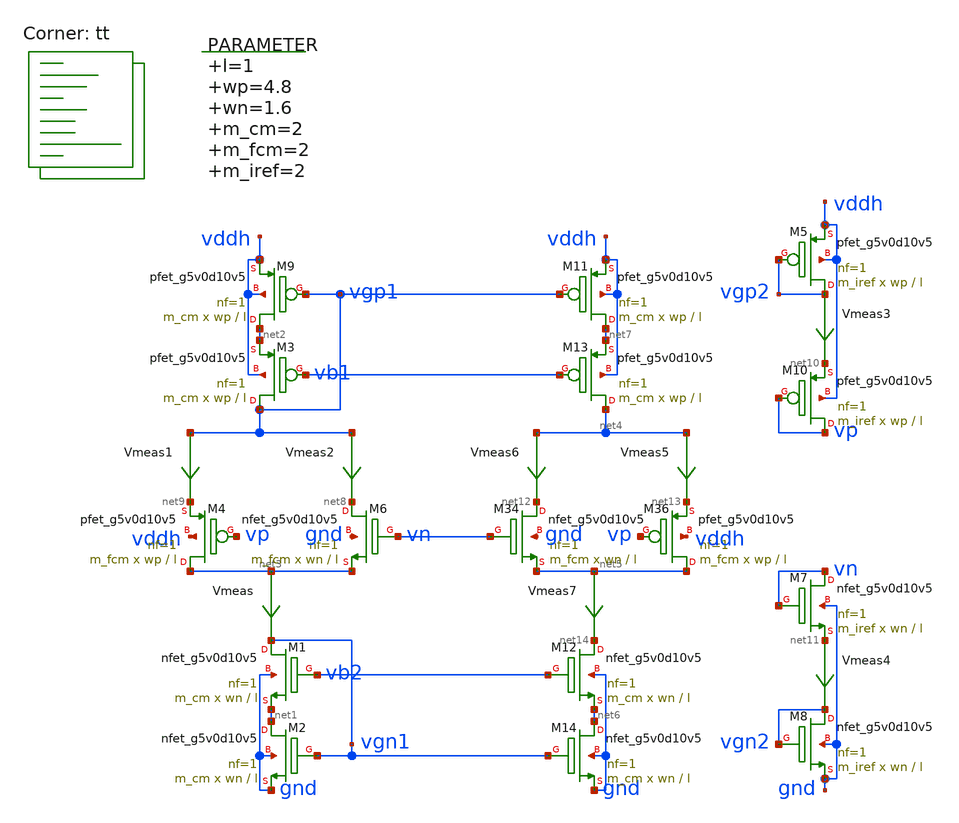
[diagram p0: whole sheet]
** sch_path: xschem/op_amp_lv_cm.sch
**.subckt op_amp_lv_cm
Vmeas net3 vgn1 0
.save i(vmeas)
XM9 net2 vgp1 vddh vddh sky130_fd_pr__pfet_g5v0d10v5 L=l W=wp nf=1 ad='int((nf+1)/2) * W/nf * 0.29' as='int((nf+2)/2) * W/nf * 0.29'
+ pd='2*int((nf+1)/2) * (W/nf + 0.29)' ps='2*int((nf+2)/2) * (W/nf + 0.29)' nrd='0.29 / W' nrs='0.29 / W'
+ sa=0 sb=0 sd=0 mult=m_cm m=m_cm
XM6 net8 vn net3 gnd sky130_fd_pr__nfet_g5v0d10v5 L=l W=wn nf=1 ad='int((nf+1)/2) * W/nf * 0.29' as='int((nf+2)/2) * W/nf * 0.29'
+ pd='2*int((nf+1)/2) * (W/nf + 0.29)' ps='2*int((nf+2)/2) * (W/nf + 0.29)' nrd='0.29 / W' nrs='0.29 / W'
+ sa=0 sb=0 sd=0 mult=m_fcm m=m_fcm
Vmeas1 vgp1 net9 0
.save i(vmeas1)
Vmeas2 vgp1 net8 0
.save i(vmeas2)
Vmeas3 vgp2 net10 0
.save i(vmeas3)
Vmeas4 net11 vgn2 0
.save i(vmeas4)
.param l=1 wp=4.8 wn=1.6 m_cm=2 m_fcm=2 m_iref=2
XM4 net3 vp net9 vddh sky130_fd_pr__pfet_g5v0d10v5 L=l W=wp nf=1 ad='int((nf+1)/2) * W/nf * 0.29' as='int((nf+2)/2) * W/nf * 0.29'
+ pd='2*int((nf+1)/2) * (W/nf + 0.29)' ps='2*int((nf+2)/2) * (W/nf + 0.29)' nrd='0.29 / W' nrs='0.29 / W'
+ sa=0 sb=0 sd=0 mult=m_fcm m=m_fcm
XM5 vgp2 vgp2 vddh vddh sky130_fd_pr__pfet_g5v0d10v5 L=l W=wp nf=1 ad='int((nf+1)/2) * W/nf * 0.29' as='int((nf+2)/2) * W/nf * 0.29'
+ pd='2*int((nf+1)/2) * (W/nf + 0.29)' ps='2*int((nf+2)/2) * (W/nf + 0.29)' nrd='0.29 / W' nrs='0.29 / W'
+ sa=0 sb=0 sd=0 mult=m_iref m=m_iref
XM1 vgn1 vb2 net1 gnd sky130_fd_pr__nfet_g5v0d10v5 L=l W=wn nf=1 ad='int((nf+1)/2) * W/nf * 0.29' as='int((nf+2)/2) * W/nf * 0.29'
+ pd='2*int((nf+1)/2) * (W/nf + 0.29)' ps='2*int((nf+2)/2) * (W/nf + 0.29)' nrd='0.29 / W' nrs='0.29 / W'
+ sa=0 sb=0 sd=0 mult=m_cm m=m_cm
XM7 vn vn net11 gnd sky130_fd_pr__nfet_g5v0d10v5 L=l W=wn nf=1 ad='int((nf+1)/2) * W/nf * 0.29' as='int((nf+2)/2) * W/nf * 0.29'
+ pd='2*int((nf+1)/2) * (W/nf + 0.29)' ps='2*int((nf+2)/2) * (W/nf + 0.29)' nrd='0.29 / W' nrs='0.29 / W'
+ sa=0 sb=0 sd=0 mult=m_iref m=m_iref
XM3 vgp1 vb1 net2 vddh sky130_fd_pr__pfet_g5v0d10v5 L=l W=wp nf=1 ad='int((nf+1)/2) * W/nf * 0.29' as='int((nf+2)/2) * W/nf * 0.29'
+ pd='2*int((nf+1)/2) * (W/nf + 0.29)' ps='2*int((nf+2)/2) * (W/nf + 0.29)' nrd='0.29 / W' nrs='0.29 / W'
+ sa=0 sb=0 sd=0 mult=m_cm m=m_cm
XM2 net1 vgn1 gnd gnd sky130_fd_pr__nfet_g5v0d10v5 L=l W=wn nf=1 ad='int((nf+1)/2) * W/nf * 0.29' as='int((nf+2)/2) * W/nf * 0.29'
+ pd='2*int((nf+1)/2) * (W/nf + 0.29)' ps='2*int((nf+2)/2) * (W/nf + 0.29)' nrd='0.29 / W' nrs='0.29 / W'
+ sa=0 sb=0 sd=0 mult=m_cm m=m_cm
XM10 vp vp net10 vddh sky130_fd_pr__pfet_g5v0d10v5 L=l W=wp nf=1 ad='int((nf+1)/2) * W/nf * 0.29' as='int((nf+2)/2) * W/nf * 0.29'
+ pd='2*int((nf+1)/2) * (W/nf + 0.29)' ps='2*int((nf+2)/2) * (W/nf + 0.29)' nrd='0.29 / W' nrs='0.29 / W'
+ sa=0 sb=0 sd=0 mult=m_iref m=m_iref
XM8 vgn2 vgn2 gnd gnd sky130_fd_pr__nfet_g5v0d10v5 L=l W=wn nf=1 ad='int((nf+1)/2) * W/nf * 0.29' as='int((nf+2)/2) * W/nf * 0.29'
+ pd='2*int((nf+1)/2) * (W/nf + 0.29)' ps='2*int((nf+2)/2) * (W/nf + 0.29)' nrd='0.29 / W' nrs='0.29 / W'
+ sa=0 sb=0 sd=0 mult=m_iref m=m_iref
XM34 net12 vn net5 gnd sky130_fd_pr__nfet_g5v0d10v5 L=l W=wn nf=1 ad='int((nf+1)/2) * W/nf * 0.29' as='int((nf+2)/2) * W/nf * 0.29'
+ pd='2*int((nf+1)/2) * (W/nf + 0.29)' ps='2*int((nf+2)/2) * (W/nf + 0.29)' nrd='0.29 / W' nrs='0.29 / W'
+ sa=0 sb=0 sd=0 mult=m_fcm m=m_fcm
XM36 net5 vp net13 vddh sky130_fd_pr__pfet_g5v0d10v5 L=l W=wp nf=1 ad='int((nf+1)/2) * W/nf * 0.29' as='int((nf+2)/2) * W/nf * 0.29'
+ pd='2*int((nf+1)/2) * (W/nf + 0.29)' ps='2*int((nf+2)/2) * (W/nf + 0.29)' nrd='0.29 / W' nrs='0.29 / W'
+ sa=0 sb=0 sd=0 mult=m_fcm m=m_fcm
Vmeas5 net4 net13 0
.save i(vmeas5)
Vmeas6 net4 net12 0
.save i(vmeas6)
Vmeas7 net5 net14 0
.save i(vmeas7)
XM11 net7 vgp1 vddh vddh sky130_fd_pr__pfet_g5v0d10v5 L=l W=wp nf=1 ad='int((nf+1)/2) * W/nf * 0.29'
+ as='int((nf+2)/2) * W/nf * 0.29' pd='2*int((nf+1)/2) * (W/nf + 0.29)' ps='2*int((nf+2)/2) * (W/nf + 0.29)'
+ nrd='0.29 / W' nrs='0.29 / W' sa=0 sb=0 sd=0 mult=m_cm m=m_cm
XM12 net14 vb2 net6 gnd sky130_fd_pr__nfet_g5v0d10v5 L=l W=wn nf=1 ad='int((nf+1)/2) * W/nf * 0.29' as='int((nf+2)/2) * W/nf * 0.29'
+ pd='2*int((nf+1)/2) * (W/nf + 0.29)' ps='2*int((nf+2)/2) * (W/nf + 0.29)' nrd='0.29 / W' nrs='0.29 / W'
+ sa=0 sb=0 sd=0 mult=m_cm m=m_cm
XM13 net4 vb1 net7 vddh sky130_fd_pr__pfet_g5v0d10v5 L=l W=wp nf=1 ad='int((nf+1)/2) * W/nf * 0.29' as='int((nf+2)/2) * W/nf * 0.29'
+ pd='2*int((nf+1)/2) * (W/nf + 0.29)' ps='2*int((nf+2)/2) * (W/nf + 0.29)' nrd='0.29 / W' nrs='0.29 / W'
+ sa=0 sb=0 sd=0 mult=m_cm m=m_cm
XM14 net6 vgn1 gnd gnd sky130_fd_pr__nfet_g5v0d10v5 L=l W=wn nf=1 ad='int((nf+1)/2) * W/nf * 0.29' as='int((nf+2)/2) * W/nf * 0.29'
+ pd='2*int((nf+1)/2) * (W/nf + 0.29)' ps='2*int((nf+2)/2) * (W/nf + 0.29)' nrd='0.29 / W' nrs='0.29 / W'
+ sa=0 sb=0 sd=0 mult=m_cm m=m_cm
**** begin user architecture code
.lib $::SKYWATER_MODELS/sky130.lib.spice tt



  .option wnflag=1
  .option safecurrents
  ********************Static Current Sources***************************
  .param iref=10u
  I1 i1 gnd iref
*  I2 i2 gnd iref
  Ip vp gnd 0.1u
  In vddh vn 0.1u
  ********************Static Voltage Sources***************************
  Vddh vddh gnd dc 5.5

*  vp vp gnd dc 2.8933
*  vn vn gnd dc 0
  vb1 vb1 gnd dc 3
  vb2 vb2 gnd dc 2
  ********************Dynamic Voltage Sources***************************
  *******Calculation**********
  .param base_f=100e3 base_t={1/base_f} base_th={base_t/2} base_d={base_th}
  .param d2_th ={base_th} d2_t={2*d2_th}
  .param d1_th ={4*d2_th} d1_t={d0_th}
  .param d0_th ={4*d1_th} d0_t={4*d0_th}

  .param d20_d ={0} d21_d={1*d2_th} d22_d={2*d2_th} d23_d={3*d2_th}
  .param d10_d ={0} d11_d={1*d1_th} d12_d={2*d1_th} d13_d={3*d1_th}
  .param d00_d ={0} d01_d={1*d0_th} d02_d={2*d0_th} d03_d={3*d0_th}
  *******Signals**********
  .param vhi=5.5
*  Vin1 b[0] gnd pulse(0 {vhi} {0} 1p 1p {10u} {20u})
*  Vin2 b[1] gnd pulse(0 {vhi} {0} 1p 1p {20u} {40u})
  ********************Simulation Commands*****************************
  .control
     reset
     save all
*     dc ip 4u 6u 0.01u
     dc vb1 2.8 3.8 0.01
*     tran 0.1n 500n
     write lv_cm-tb.raw
     set appendwrite
*    quit 0
  .endc



**** end user architecture code
**.ends
.end
